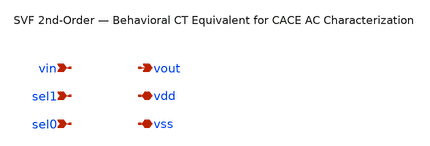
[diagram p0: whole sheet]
** sch_path: verification/svf_2nd/xschem/svf_2nd.sch
**.subckt svf_2nd vin vout sel1 sel0 vdd vss
*.ipin vin
*.opin vout
*.ipin sel1
*.ipin sel0
*.iopin vdd
*.iopin vss
**** begin user architecture code


.param vcm_val = 0.6
.param vdd_sq_val = 1.44
.param c_int_val = 1.1e-12
.param vdd_val = 1.2

* ==== Integrator 1 (inverting): produces BP ====
Eoa1  bp_raw 0 vcm1 vg1 10000
Vcm1  vcm1 0 {vcm_val}
Rout1 bp_raw bp 100
Cint1 vg1 bp {c_int_val}

* Input resistor (Vin -> vg1)
Rin1 vin vg1 {r_eff_val}
* LP negative feedback resistor (LP -> vg1)
Rfb lp vg1 {r_eff_val}
* Damping resistor (BP -> vg1)
Rq bp vg1 {r_q_val}

* ==== Unity-gain inverter: LP_bar -> LP ====
Eoa_inv  lp_raw 0 vcm_inv vg_inv 10000
Vcm_inv  vcm_inv 0 {vcm_val}
Rout_inv lp_raw lp 100
Rinv_in  lp_bar vg_inv 100k
Rinv_fb  vg_inv lp 100k

* ==== Integrator 2 (inverting): produces LP_bar ====
Eoa2  lpbar_raw 0 vcm2 vg2 10000
Vcm2  vcm2 0 {vcm_val}
Rout2 lpbar_raw lp_bar 100
Cint2 vg2 lp_bar {c_int_val}
Rin2  bp vg2 {r_eff_val}

* ==== HP output (behavioral) ====
Bhp hp 0 V = v(vin) + v(lp) + v(bp)

* ==== 4:1 Output Mux (behavioral) ====
Bsel_hp  sel_hp  0 V = ({vdd_val}-v(sel1))*({vdd_val}-v(sel0))/{vdd_sq_val}
Bsel_bp  sel_bp  0 V = ({vdd_val}-v(sel1))*v(sel0)/{vdd_sq_val}
Bsel_lp  sel_lp  0 V = v(sel1)*({vdd_val}-v(sel0))/{vdd_sq_val}
Bsel_byp sel_byp 0 V = v(sel1)*v(sel0)/{vdd_sq_val}

Bmux vmux 0 V = v(hp)*v(sel_hp)+v(bp)*v(sel_bp)+v(lp)*v(sel_lp)+v(vin)*v(sel_byp)
Rmux vmux vout 100


**** end user architecture code
**.ends
.end
